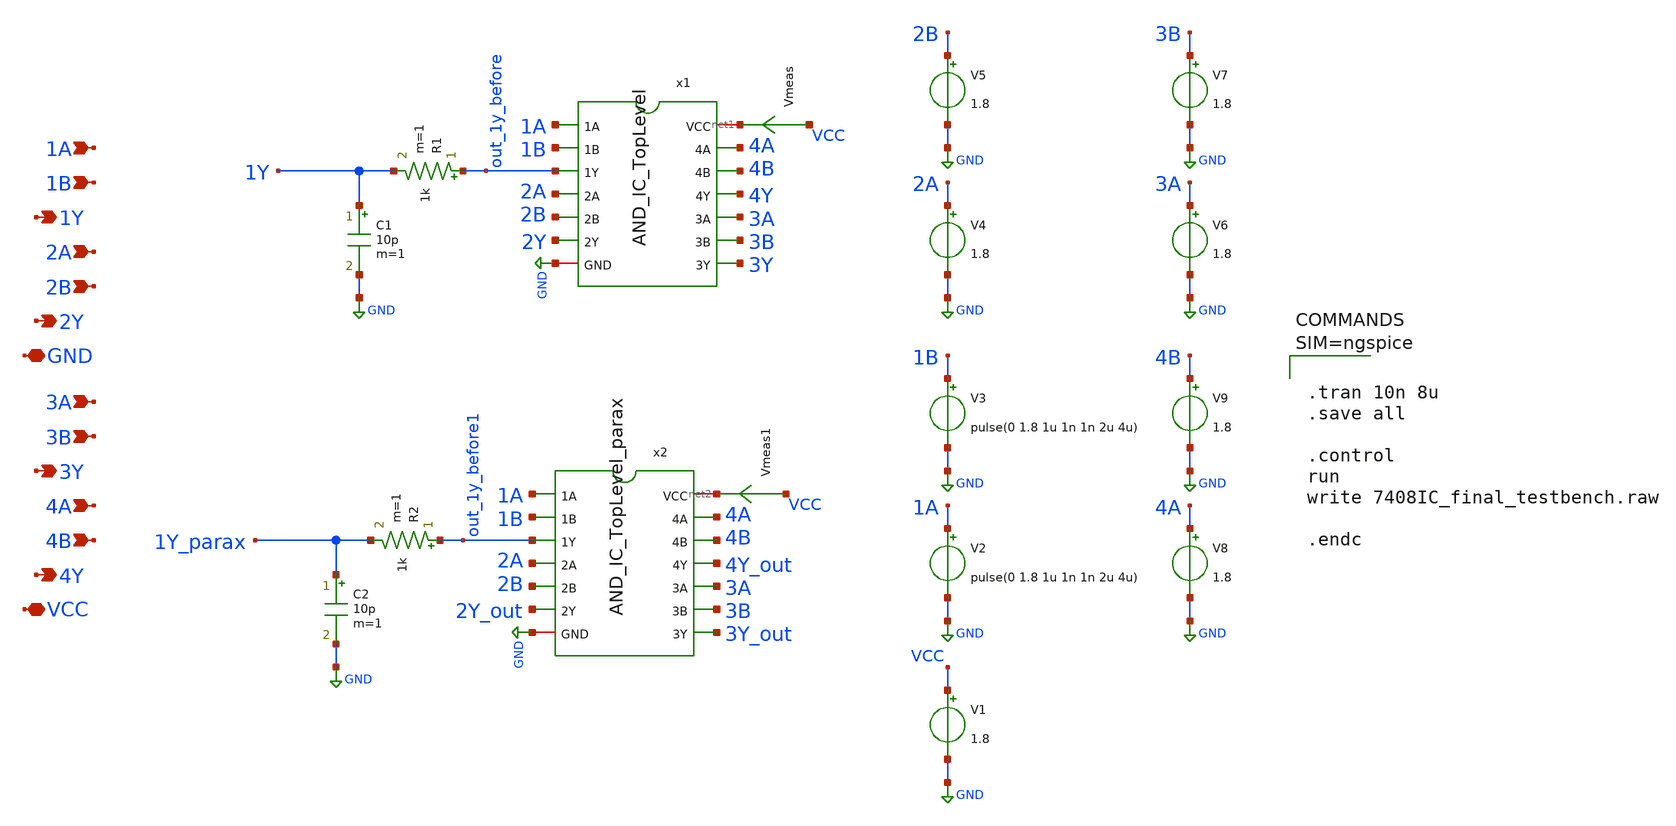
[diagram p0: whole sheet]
** sch_path: xschem/ic_7408_testbench.sch
**.subckt ic_7408_testbench 1A GND 1Y 1B 2A 2B 3A 3B 4A 4B 2Y 3Y 4Y VCC
*.ipin 1A
*.iopin GND
*.opin 1Y
*.ipin 1B
*.ipin 2A
*.ipin 2B
*.ipin 3A
*.ipin 3B
*.ipin 4A
*.ipin 4B
*.opin 2Y
*.opin 3Y
*.opin 4Y
*.iopin VCC
V1 VCC GND 1.8
V2 1A GND pulse(0 1.8 1u 1n 1n 2u 4u)
V3 1B GND pulse(0 1.8 1u 1n 1n 2u 4u)
R1 out_1y_before 1Y 1k m=1
C1 1Y GND 10p m=1
x1 1A 1B out_1y_before 2A 2B 2Y GND 3A 3B 3Y 4A 4B 4Y net1 AND_IC_TopLevel
Vmeas VCC net1 0
.save i(vmeas)
V4 2A GND 1.8
V5 2B GND 1.8
V6 3A GND 1.8
V7 3B GND 1.8
V8 4A GND 1.8
V9 4B GND 1.8
R2 out_1y_before1 1Y_parax 1k m=1
C2 1Y_parax GND 10p m=1
x2 1A 1B out_1y_before1 2A 2B 2Y_out GND 3A 3B 3Y_out 4A 4B 4Y_out net2 AND_IC_TopLevel_parax
Vmeas1 VCC net2 0
.save i(vmeas1)
**** begin user architecture code

** opencircuitdesign pdks install
.lib $::SKYWATER_MODELS/sky130.lib.spice tt





.tran 10n 8u
.save all

.control
run
write 7408IC_final_testbench.raw

.endc



**** end user architecture code
**.ends

* expanding   symbol:  AND_IC_TopLevel.sym # of pins=14
** sym_path: xschem/AND_IC_TopLevel.sym
** sch_path: xschem/AND_IC_TopLevel.sch
.subckt AND_IC_TopLevel 1A 1B 1Y 2A 2B 2Y GND 3A 3B 3Y 4A 4B 4Y VCC
*.ipin 1A
*.iopin GND
*.opin 1Y
*.ipin 1B
*.ipin 2A
*.ipin 2B
*.ipin 3A
*.ipin 3B
*.ipin 4A
*.ipin 4B
*.opin 2Y
*.opin 3Y
*.opin 4Y
*.iopin VCC
x1 1A 1B 1Y VCC GND ic_7804_AND
x2 2A 2B 2Y VCC GND ic_7804_AND
x3 3A 3B 3Y VCC GND ic_7804_AND
x4 4A 4B 4Y VCC GND ic_7804_AND
.ends


* expanding   symbol:  AND_IC_TopLevel_parax.sym # of pins=14
** sym_path: xschem/AND_IC_TopLevel.sym
.include [file normalize ../mag/AND_IC_TopLevel.sim.spice]

* expanding   symbol:  ic_7804_AND.sym # of pins=5
** sym_path: xschem/ic_7804_AND.sym
** sch_path: xschem/ic_7804_AND.sch
.subckt ic_7804_AND A B Y VCC GND
*.ipin A
*.opin Y
*.ipin B
*.iopin VCC
*.iopin GND
XM2 net1 A VCC VCC sky130_fd_pr__pfet_01v8 L=0.15 W=2 nf=1 ad='int((nf+1)/2) * W/nf * 0.29' as='int((nf+2)/2) * W/nf * 0.29'
+ pd='2*int((nf+1)/2) * (W/nf + 0.29)' ps='2*int((nf+2)/2) * (W/nf + 0.29)' nrd='0.29 / W' nrs='0.29 / W'
+ sa=0 sb=0 sd=0 mult=1 m=1
XM3 net1 B VCC VCC sky130_fd_pr__pfet_01v8 L=0.15 W=2 nf=1 ad='int((nf+1)/2) * W/nf * 0.29' as='int((nf+2)/2) * W/nf * 0.29'
+ pd='2*int((nf+1)/2) * (W/nf + 0.29)' ps='2*int((nf+2)/2) * (W/nf + 0.29)' nrd='0.29 / W' nrs='0.29 / W'
+ sa=0 sb=0 sd=0 mult=1 m=1
XM5 Y net1 VCC VCC sky130_fd_pr__pfet_01v8 L=0.15 W=2 nf=1 ad='int((nf+1)/2) * W/nf * 0.29' as='int((nf+2)/2) * W/nf * 0.29'
+ pd='2*int((nf+1)/2) * (W/nf + 0.29)' ps='2*int((nf+2)/2) * (W/nf + 0.29)' nrd='0.29 / W' nrs='0.29 / W'
+ sa=0 sb=0 sd=0 mult=1 m=1
XM1 net1 A net2 GND sky130_fd_pr__nfet_01v8 L=0.15 W=1 nf=1 ad='int((nf+1)/2) * W/nf * 0.29' as='int((nf+2)/2) * W/nf * 0.29'
+ pd='2*int((nf+1)/2) * (W/nf + 0.29)' ps='2*int((nf+2)/2) * (W/nf + 0.29)' nrd='0.29 / W' nrs='0.29 / W'
+ sa=0 sb=0 sd=0 mult=1 m=1
XM4 net2 B GND GND sky130_fd_pr__nfet_01v8 L=0.15 W=1 nf=1 ad='int((nf+1)/2) * W/nf * 0.29' as='int((nf+2)/2) * W/nf * 0.29'
+ pd='2*int((nf+1)/2) * (W/nf + 0.29)' ps='2*int((nf+2)/2) * (W/nf + 0.29)' nrd='0.29 / W' nrs='0.29 / W'
+ sa=0 sb=0 sd=0 mult=1 m=1
XM6 Y net1 GND GND sky130_fd_pr__nfet_01v8 L=0.15 W=1 nf=1 ad='int((nf+1)/2) * W/nf * 0.29' as='int((nf+2)/2) * W/nf * 0.29'
+ pd='2*int((nf+1)/2) * (W/nf + 0.29)' ps='2*int((nf+2)/2) * (W/nf + 0.29)' nrd='0.29 / W' nrs='0.29 / W'
+ sa=0 sb=0 sd=0 mult=1 m=1
.ends

.GLOBAL GND
.end
